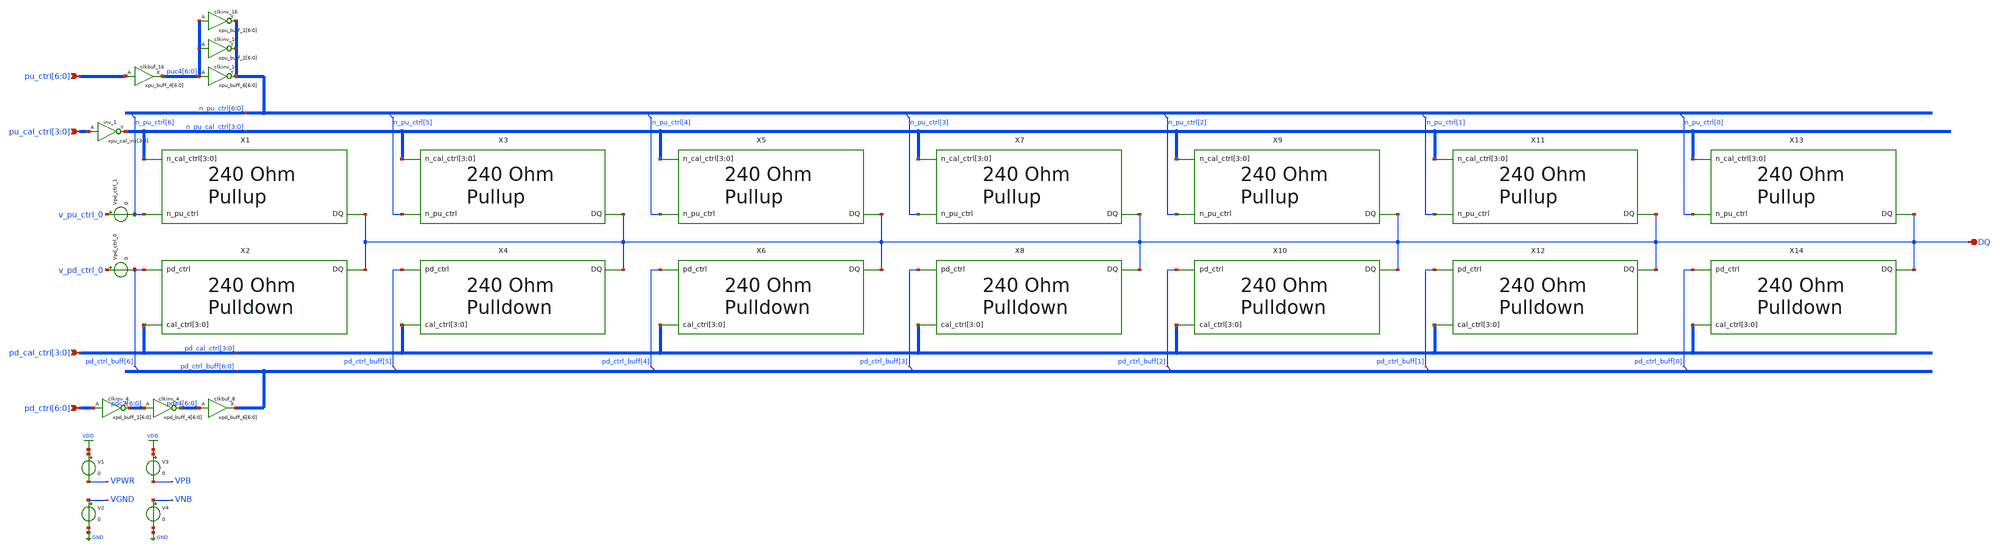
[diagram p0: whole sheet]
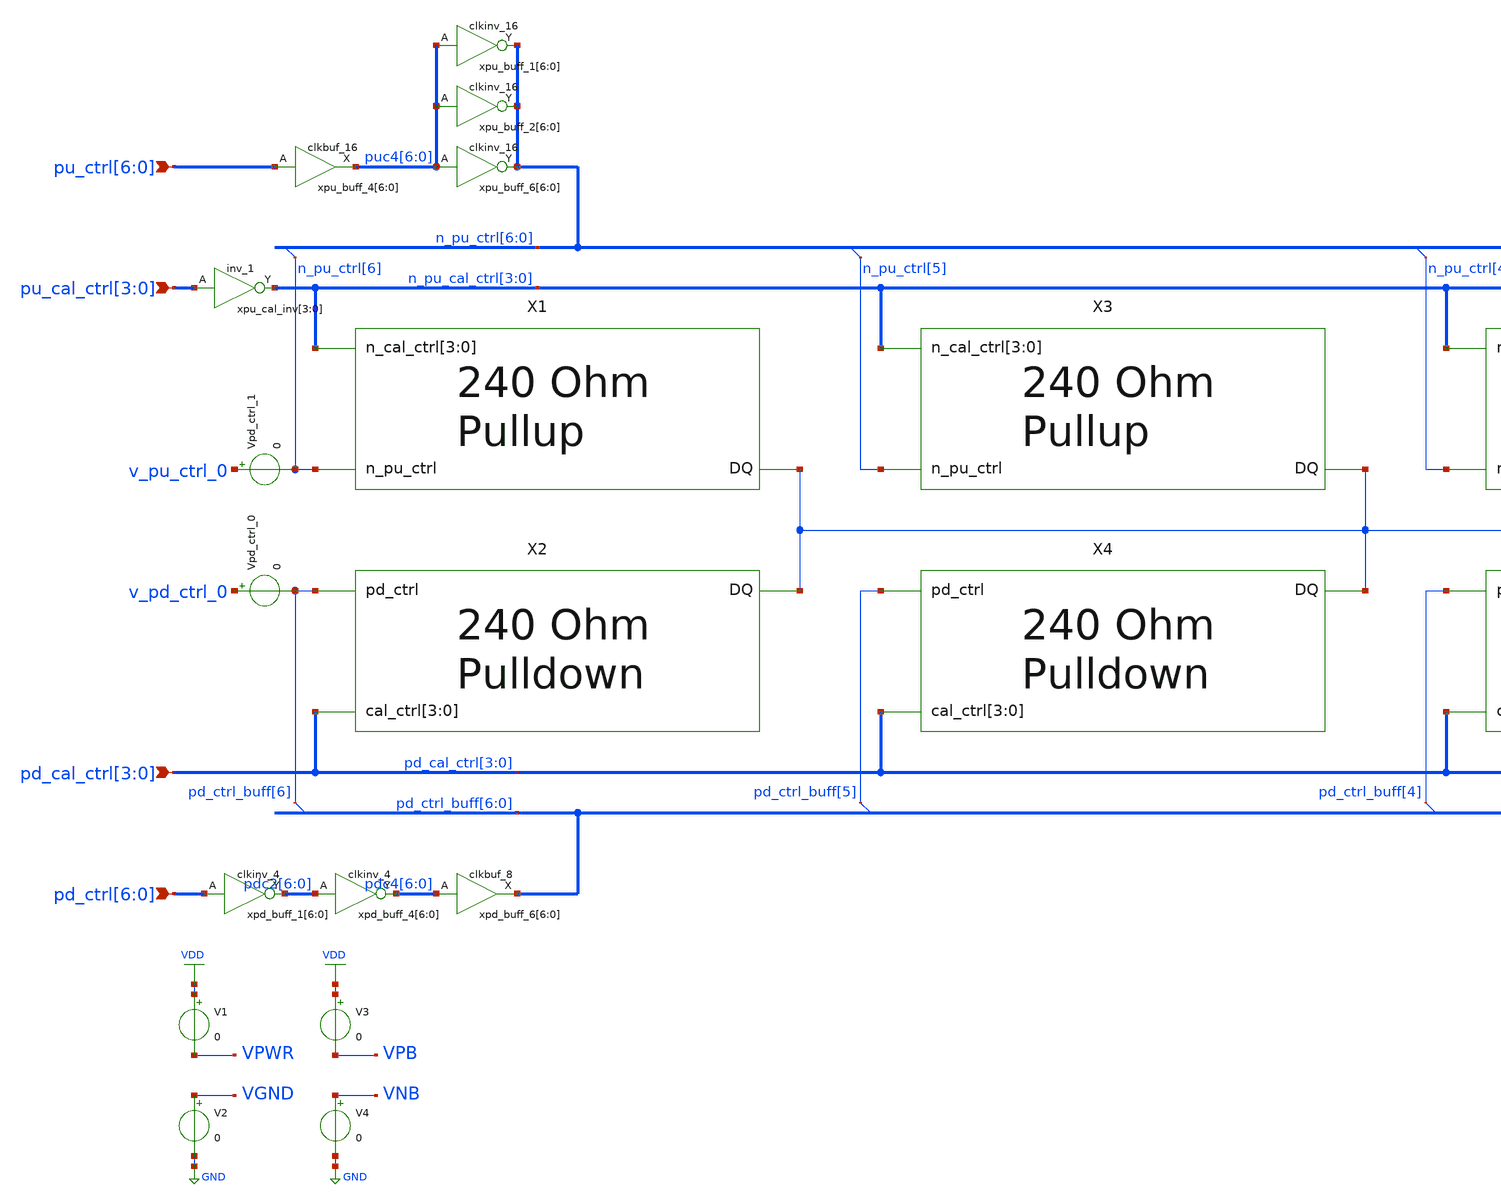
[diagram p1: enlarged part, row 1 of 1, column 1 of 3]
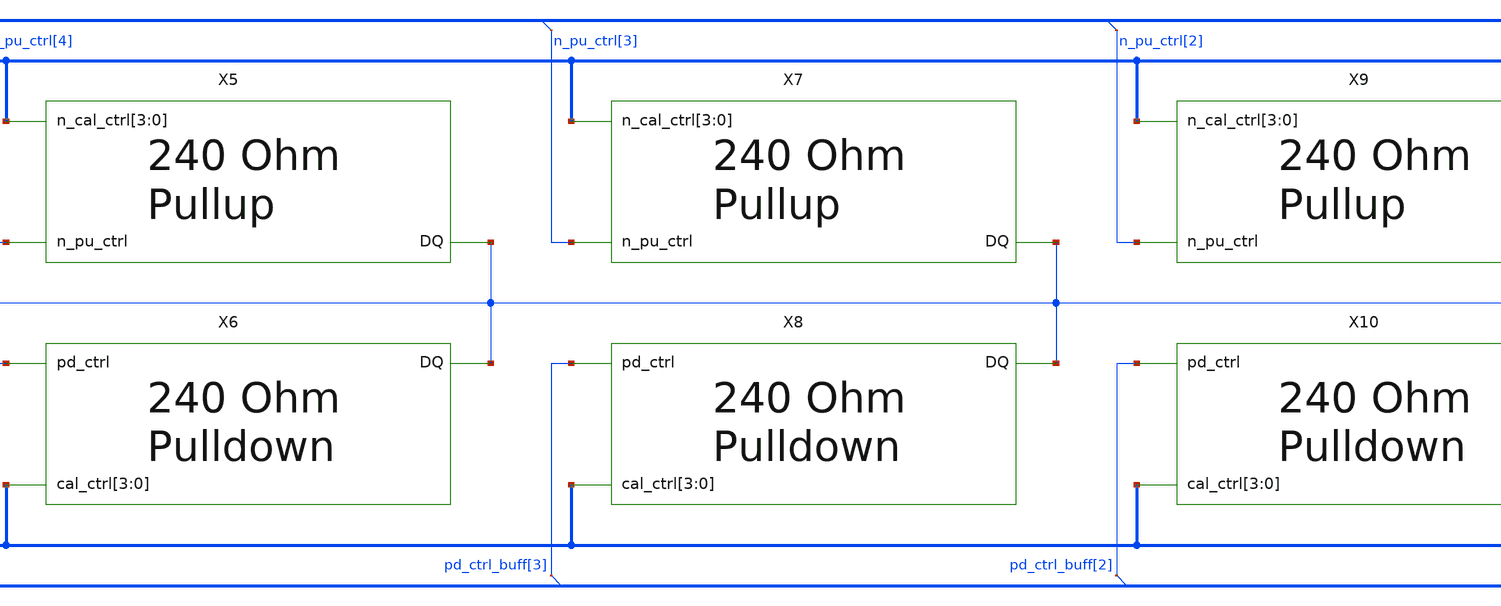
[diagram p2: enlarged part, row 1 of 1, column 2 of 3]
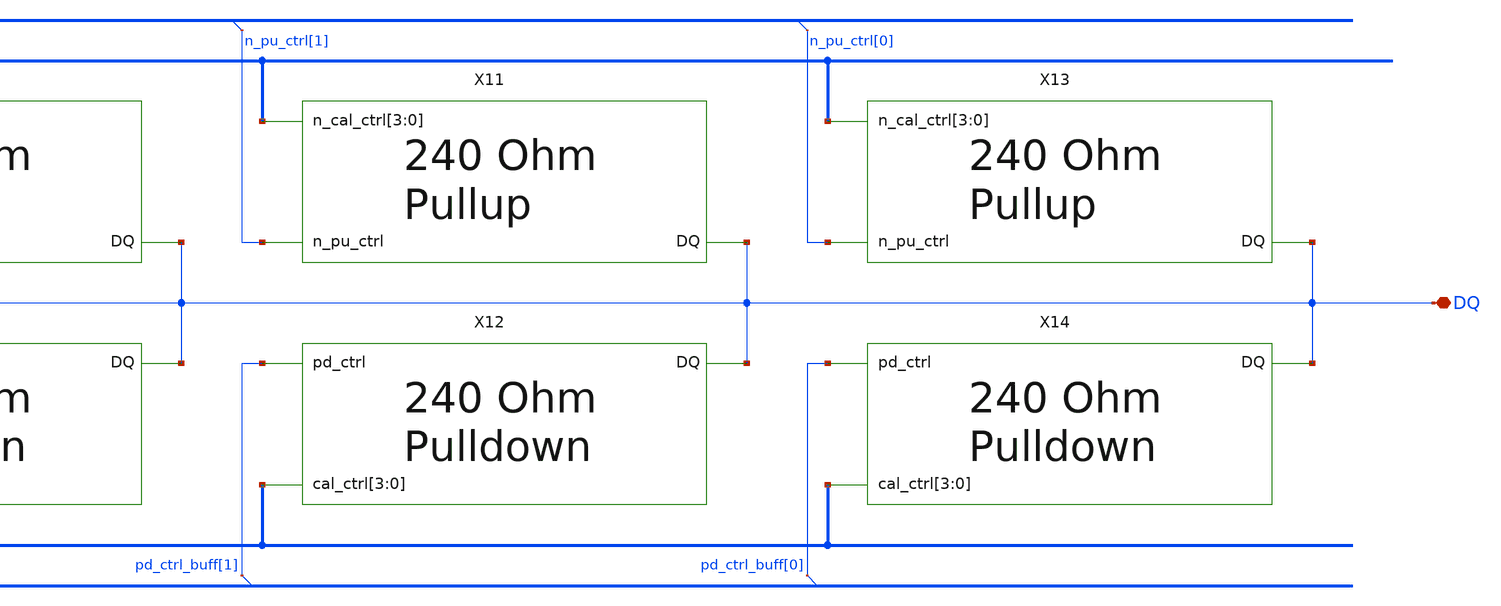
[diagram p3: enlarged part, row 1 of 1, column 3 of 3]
** sch_path: schem/SSTL.sch
* Copyright 2021 Stefan Frederik Schippers
* Licensed under the Apache License, Version 2.0 (the "License");
* you may not use this file except in compliance with the License.
* You may obtain a copy of the License at
* https://www.apache.org/licenses/LICENSE-2.0
* Unless required by applicable law or agreed to in writing, software
* distributed under the License is distributed on an "AS IS" BASIS,
* WITHOUT WARRANTIES OR CONDITIONS OF ANY KIND, either express or implied.
* See the License for the specific language governing permissions and
* limitations under the License.
**.subckt SSTL DQ pu_cal_ctrl[3],pu_cal_ctrl[2],pu_cal_ctrl[1],pu_cal_ctrl[0]
*+ pd_cal_ctrl[3],pd_cal_ctrl[2],pd_cal_ctrl[1],pd_cal_ctrl[0] pu_ctrl[6],pu_ctrl[5],pu_ctrl[4],pu_ctrl[3],pu_ctrl[2],pu_ctrl[1],pu_ctrl[0]
*+ pd_ctrl[6],pd_ctrl[5],pd_ctrl[4],pd_ctrl[3],pd_ctrl[2],pd_ctrl[1],pd_ctrl[0]
*.iopin DQ
*.ipin pu_cal_ctrl[3],pu_cal_ctrl[2],pu_cal_ctrl[1],pu_cal_ctrl[0]
*.ipin pd_cal_ctrl[3],pd_cal_ctrl[2],pd_cal_ctrl[1],pd_cal_ctrl[0]
*.ipin pu_ctrl[6],pu_ctrl[5],pu_ctrl[4],pu_ctrl[3],pu_ctrl[2],pu_ctrl[1],pu_ctrl[0]
*.ipin pd_ctrl[6],pd_ctrl[5],pd_ctrl[4],pd_ctrl[3],pd_ctrl[2],pd_ctrl[1],pd_ctrl[0]
X1 DQ n_pu_ctrl[6] n_pu_cal_ctrl[3] n_pu_cal_ctrl[2] n_pu_cal_ctrl[1] n_pu_cal_ctrl[0] p-leg
X2 DQ pd_ctrl_buff[6] pd_cal_ctrl[3] pd_cal_ctrl[2] pd_cal_ctrl[1] pd_cal_ctrl[0] n-leg
X3 DQ n_pu_ctrl[5] n_pu_cal_ctrl[3] n_pu_cal_ctrl[2] n_pu_cal_ctrl[1] n_pu_cal_ctrl[0] p-leg
X4 DQ pd_ctrl_buff[5] pd_cal_ctrl[3] pd_cal_ctrl[2] pd_cal_ctrl[1] pd_cal_ctrl[0] n-leg
X5 DQ n_pu_ctrl[4] n_pu_cal_ctrl[3] n_pu_cal_ctrl[2] n_pu_cal_ctrl[1] n_pu_cal_ctrl[0] p-leg
X6 DQ pd_ctrl_buff[4] pd_cal_ctrl[3] pd_cal_ctrl[2] pd_cal_ctrl[1] pd_cal_ctrl[0] n-leg
X7 DQ n_pu_ctrl[3] n_pu_cal_ctrl[3] n_pu_cal_ctrl[2] n_pu_cal_ctrl[1] n_pu_cal_ctrl[0] p-leg
X8 DQ pd_ctrl_buff[3] pd_cal_ctrl[3] pd_cal_ctrl[2] pd_cal_ctrl[1] pd_cal_ctrl[0] n-leg
X9 DQ n_pu_ctrl[2] n_pu_cal_ctrl[3] n_pu_cal_ctrl[2] n_pu_cal_ctrl[1] n_pu_cal_ctrl[0] p-leg
X10 DQ pd_ctrl_buff[2] pd_cal_ctrl[3] pd_cal_ctrl[2] pd_cal_ctrl[1] pd_cal_ctrl[0] n-leg
X11 DQ n_pu_ctrl[1] n_pu_cal_ctrl[3] n_pu_cal_ctrl[2] n_pu_cal_ctrl[1] n_pu_cal_ctrl[0] p-leg
X12 DQ pd_ctrl_buff[1] pd_cal_ctrl[3] pd_cal_ctrl[2] pd_cal_ctrl[1] pd_cal_ctrl[0] n-leg
X13 DQ n_pu_ctrl[0] n_pu_cal_ctrl[3] n_pu_cal_ctrl[2] n_pu_cal_ctrl[1] n_pu_cal_ctrl[0] p-leg
X14 DQ pd_ctrl_buff[0] pd_cal_ctrl[3] pd_cal_ctrl[2] pd_cal_ctrl[1] pd_cal_ctrl[0] n-leg
xpd_buff_4[6] pdc2[6] VGND VNB VPB VPWR pdc4[6] sky130_fd_sc_hd__clkinv_4
xpd_buff_4[5] pdc2[5] VGND VNB VPB VPWR pdc4[5] sky130_fd_sc_hd__clkinv_4
xpd_buff_4[4] pdc2[4] VGND VNB VPB VPWR pdc4[4] sky130_fd_sc_hd__clkinv_4
xpd_buff_4[3] pdc2[3] VGND VNB VPB VPWR pdc4[3] sky130_fd_sc_hd__clkinv_4
xpd_buff_4[2] pdc2[2] VGND VNB VPB VPWR pdc4[2] sky130_fd_sc_hd__clkinv_4
xpd_buff_4[1] pdc2[1] VGND VNB VPB VPWR pdc4[1] sky130_fd_sc_hd__clkinv_4
xpd_buff_4[0] pdc2[0] VGND VNB VPB VPWR pdc4[0] sky130_fd_sc_hd__clkinv_4
xpd_buff_6[6] pdc4[6] VGND VNB VPB VPWR pd_ctrl_buff[6] sky130_fd_sc_hd__clkbuf_8
xpd_buff_6[5] pdc4[5] VGND VNB VPB VPWR pd_ctrl_buff[5] sky130_fd_sc_hd__clkbuf_8
xpd_buff_6[4] pdc4[4] VGND VNB VPB VPWR pd_ctrl_buff[4] sky130_fd_sc_hd__clkbuf_8
xpd_buff_6[3] pdc4[3] VGND VNB VPB VPWR pd_ctrl_buff[3] sky130_fd_sc_hd__clkbuf_8
xpd_buff_6[2] pdc4[2] VGND VNB VPB VPWR pd_ctrl_buff[2] sky130_fd_sc_hd__clkbuf_8
xpd_buff_6[1] pdc4[1] VGND VNB VPB VPWR pd_ctrl_buff[1] sky130_fd_sc_hd__clkbuf_8
xpd_buff_6[0] pdc4[0] VGND VNB VPB VPWR pd_ctrl_buff[0] sky130_fd_sc_hd__clkbuf_8
xpu_buff_4[6] pu_ctrl[6] VGND VNB VPB VPWR puc4[6] sky130_fd_sc_hd__clkbuf_16
xpu_buff_4[5] pu_ctrl[5] VGND VNB VPB VPWR puc4[5] sky130_fd_sc_hd__clkbuf_16
xpu_buff_4[4] pu_ctrl[4] VGND VNB VPB VPWR puc4[4] sky130_fd_sc_hd__clkbuf_16
xpu_buff_4[3] pu_ctrl[3] VGND VNB VPB VPWR puc4[3] sky130_fd_sc_hd__clkbuf_16
xpu_buff_4[2] pu_ctrl[2] VGND VNB VPB VPWR puc4[2] sky130_fd_sc_hd__clkbuf_16
xpu_buff_4[1] pu_ctrl[1] VGND VNB VPB VPWR puc4[1] sky130_fd_sc_hd__clkbuf_16
xpu_buff_4[0] pu_ctrl[0] VGND VNB VPB VPWR puc4[0] sky130_fd_sc_hd__clkbuf_16
xpu_buff_6[6] puc4[6] VGND VNB VPB VPWR n_pu_ctrl[6] sky130_fd_sc_hd__clkinv_16
xpu_buff_6[5] puc4[5] VGND VNB VPB VPWR n_pu_ctrl[5] sky130_fd_sc_hd__clkinv_16
xpu_buff_6[4] puc4[4] VGND VNB VPB VPWR n_pu_ctrl[4] sky130_fd_sc_hd__clkinv_16
xpu_buff_6[3] puc4[3] VGND VNB VPB VPWR n_pu_ctrl[3] sky130_fd_sc_hd__clkinv_16
xpu_buff_6[2] puc4[2] VGND VNB VPB VPWR n_pu_ctrl[2] sky130_fd_sc_hd__clkinv_16
xpu_buff_6[1] puc4[1] VGND VNB VPB VPWR n_pu_ctrl[1] sky130_fd_sc_hd__clkinv_16
xpu_buff_6[0] puc4[0] VGND VNB VPB VPWR n_pu_ctrl[0] sky130_fd_sc_hd__clkinv_16
xpu_cal_inv[3] pu_cal_ctrl[3] VGND VNB VPB VPWR n_pu_cal_ctrl[3] sky130_fd_sc_hd__inv_1
xpu_cal_inv[2] pu_cal_ctrl[2] VGND VNB VPB VPWR n_pu_cal_ctrl[2] sky130_fd_sc_hd__inv_1
xpu_cal_inv[1] pu_cal_ctrl[1] VGND VNB VPB VPWR n_pu_cal_ctrl[1] sky130_fd_sc_hd__inv_1
xpu_cal_inv[0] pu_cal_ctrl[0] VGND VNB VPB VPWR n_pu_cal_ctrl[0] sky130_fd_sc_hd__inv_1
V1 VDD VPWR 0
V2 VGND GND 0
V3 VDD VPB 0
V4 VNB GND 0
Vpd_ctrl_0 v_pd_ctrl_0 pd_ctrl_buff[6] 0
Vpd_ctrl_1 v_pu_ctrl_0 n_pu_ctrl[6] 0
xpu_buff_2[6] puc4[6] VGND VNB VPB VPWR n_pu_ctrl[6] sky130_fd_sc_hd__clkinv_16
xpu_buff_2[5] puc4[5] VGND VNB VPB VPWR n_pu_ctrl[5] sky130_fd_sc_hd__clkinv_16
xpu_buff_2[4] puc4[4] VGND VNB VPB VPWR n_pu_ctrl[4] sky130_fd_sc_hd__clkinv_16
xpu_buff_2[3] puc4[3] VGND VNB VPB VPWR n_pu_ctrl[3] sky130_fd_sc_hd__clkinv_16
xpu_buff_2[2] puc4[2] VGND VNB VPB VPWR n_pu_ctrl[2] sky130_fd_sc_hd__clkinv_16
xpu_buff_2[1] puc4[1] VGND VNB VPB VPWR n_pu_ctrl[1] sky130_fd_sc_hd__clkinv_16
xpu_buff_2[0] puc4[0] VGND VNB VPB VPWR n_pu_ctrl[0] sky130_fd_sc_hd__clkinv_16
xpd_buff_1[6] pd_ctrl[6] VGND VNB VPB VPWR pdc2[6] sky130_fd_sc_hd__clkinv_4
xpd_buff_1[5] pd_ctrl[5] VGND VNB VPB VPWR pdc2[5] sky130_fd_sc_hd__clkinv_4
xpd_buff_1[4] pd_ctrl[4] VGND VNB VPB VPWR pdc2[4] sky130_fd_sc_hd__clkinv_4
xpd_buff_1[3] pd_ctrl[3] VGND VNB VPB VPWR pdc2[3] sky130_fd_sc_hd__clkinv_4
xpd_buff_1[2] pd_ctrl[2] VGND VNB VPB VPWR pdc2[2] sky130_fd_sc_hd__clkinv_4
xpd_buff_1[1] pd_ctrl[1] VGND VNB VPB VPWR pdc2[1] sky130_fd_sc_hd__clkinv_4
xpd_buff_1[0] pd_ctrl[0] VGND VNB VPB VPWR pdc2[0] sky130_fd_sc_hd__clkinv_4
xpu_buff_1[6] puc4[6] VGND VNB VPB VPWR n_pu_ctrl[6] sky130_fd_sc_hd__clkinv_16
xpu_buff_1[5] puc4[5] VGND VNB VPB VPWR n_pu_ctrl[5] sky130_fd_sc_hd__clkinv_16
xpu_buff_1[4] puc4[4] VGND VNB VPB VPWR n_pu_ctrl[4] sky130_fd_sc_hd__clkinv_16
xpu_buff_1[3] puc4[3] VGND VNB VPB VPWR n_pu_ctrl[3] sky130_fd_sc_hd__clkinv_16
xpu_buff_1[2] puc4[2] VGND VNB VPB VPWR n_pu_ctrl[2] sky130_fd_sc_hd__clkinv_16
xpu_buff_1[1] puc4[1] VGND VNB VPB VPWR n_pu_ctrl[1] sky130_fd_sc_hd__clkinv_16
xpu_buff_1[0] puc4[0] VGND VNB VPB VPWR n_pu_ctrl[0] sky130_fd_sc_hd__clkinv_16
**.ends

* expanding   symbol:  p-leg.sym # of pins=3
** sym_path: schem/p-leg.sym
** sch_path: schem/p-leg.sch
.subckt p-leg DQ n_pu_ctrl n_cal_ctrl[3] n_cal_ctrl[2] n_cal_ctrl[1] n_cal_ctrl[0]
*.ipin n_cal_ctrl[3],n_cal_ctrl[2],n_cal_ctrl[1],n_cal_ctrl[0]
*.ipin n_pu_ctrl
*.iopin DQ
XR1 DQ net1 sky130_fd_pr__res_generic_po W=0.33 L=1.8 m=1
XMpullup net1 n_pu_ctrl VDD VDD sky130_fd_pr__pfet_01v8_lvt L=0.35 W=1 nf=1 ad='int((nf+1)/2) * W/nf * 0.29'
+ as='int((nf+2)/2) * W/nf * 0.29' pd='2*int((nf+1)/2) * (W/nf + 0.29)' ps='2*int((nf+2)/2) * (W/nf + 0.29)'
+ nrd='0.29 / W' nrs='0.29 / W' sa=0 sb=0 sd=0 mult=128 m=128
XMctrltot VDD n_cal_ctrl[0] VDD VDD sky130_fd_pr__pfet_01v8_lvt L=0.35 W=1 nf=1 ad='int((nf+1)/2) * W/nf * 0.29'
+ as='int((nf+2)/2) * W/nf * 0.29' pd='2*int((nf+1)/2) * (W/nf + 0.29)' ps='2*int((nf+2)/2) * (W/nf + 0.29)'
+ nrd='0.29 / W' nrs='0.29 / W' sa=0 sb=0 sd=0 mult=120 m=120
XMctrl0 DQ n_cal_ctrl[0] net1 VDD sky130_fd_pr__pfet_01v8_lvt L=0.35 W=1 nf=1 ad='int((nf+1)/2) * W/nf * 0.29'
+ as='int((nf+2)/2) * W/nf * 0.29' pd='2*int((nf+1)/2) * (W/nf + 0.29)' ps='2*int((nf+2)/2) * (W/nf + 0.29)'
+ nrd='0.29 / W' nrs='0.29 / W' sa=0 sb=0 sd=0 mult=48 m=48
XMctrl1 DQ n_cal_ctrl[1] net1 VDD sky130_fd_pr__pfet_01v8_lvt L=0.35 W=1 nf=1 ad='int((nf+1)/2) * W/nf * 0.29'
+ as='int((nf+2)/2) * W/nf * 0.29' pd='2*int((nf+1)/2) * (W/nf + 0.29)' ps='2*int((nf+2)/2) * (W/nf + 0.29)'
+ nrd='0.29 / W' nrs='0.29 / W' sa=0 sb=0 sd=0 mult=16 m=16
XMctrl2 DQ n_cal_ctrl[2] net1 VDD sky130_fd_pr__pfet_01v8_lvt L=0.35 W=1 nf=1 ad='int((nf+1)/2) * W/nf * 0.29'
+ as='int((nf+2)/2) * W/nf * 0.29' pd='2*int((nf+1)/2) * (W/nf + 0.29)' ps='2*int((nf+2)/2) * (W/nf + 0.29)'
+ nrd='0.29 / W' nrs='0.29 / W' sa=0 sb=0 sd=0 mult=8 m=8
XMctrl3 DQ n_cal_ctrl[3] net1 VDD sky130_fd_pr__pfet_01v8_lvt L=0.35 W=1 nf=1 ad='int((nf+1)/2) * W/nf * 0.29'
+ as='int((nf+2)/2) * W/nf * 0.29' pd='2*int((nf+1)/2) * (W/nf + 0.29)' ps='2*int((nf+2)/2) * (W/nf + 0.29)'
+ nrd='0.29 / W' nrs='0.29 / W' sa=0 sb=0 sd=0 mult=4 m=4
.ends


* expanding   symbol:  n-leg.sym # of pins=3
** sym_path: schem/n-leg.sym
** sch_path: schem/n-leg.sch
.subckt n-leg DQ pd_ctrl cal_ctrl[3] cal_ctrl[2] cal_ctrl[1] cal_ctrl[0]
*.iopin DQ
*.ipin pd_ctrl
*.ipin cal_ctrl[3],cal_ctrl[2],cal_ctrl[1],cal_ctrl[0]
XR1 vpulldown DQ sky130_fd_pr__res_generic_po W=0.33 L=1.7 m=1
Xn1 vpulldown pd_ctrl GND GND sky130_fd_pr__nfet_01v8 L=0.15 W=0.65 nf=1 ad='int((nf+1)/2) * W/nf * 0.29'
+ as='int((nf+2)/2) * W/nf * 0.29' pd='2*int((nf+1)/2) * (W/nf + 0.29)' ps='2*int((nf+2)/2) * (W/nf + 0.29)'
+ nrd='0.29 / W' nrs='0.29 / W' sa=0 sb=0 sd=0 mult=48 m=48
Xnctrl0 DQ cal_ctrl[0] vpulldown GND sky130_fd_pr__nfet_01v8 L=0.15 W=0.65 nf=1 ad='int((nf+1)/2) * W/nf * 0.29'
+ as='int((nf+2)/2) * W/nf * 0.29' pd='2*int((nf+1)/2) * (W/nf + 0.29)' ps='2*int((nf+2)/2) * (W/nf + 0.29)'
+ nrd='0.29 / W' nrs='0.29 / W' sa=0 sb=0 sd=0 mult=6 m=6
Xnctrl1 DQ cal_ctrl[1] vpulldown GND sky130_fd_pr__nfet_01v8 L=0.15 W=0.65 nf=1 ad='int((nf+1)/2) * W/nf * 0.29'
+ as='int((nf+2)/2) * W/nf * 0.29' pd='2*int((nf+1)/2) * (W/nf + 0.29)' ps='2*int((nf+2)/2) * (W/nf + 0.29)'
+ nrd='0.29 / W' nrs='0.29 / W' sa=0 sb=0 sd=0 mult=3 m=3
Xnctrl2 DQ cal_ctrl[2] vpulldown GND sky130_fd_pr__nfet_01v8 L=0.15 W=0.975 nf=1 ad='int((nf+1)/2) * W/nf * 0.29'
+ as='int((nf+2)/2) * W/nf * 0.29' pd='2*int((nf+1)/2) * (W/nf + 0.29)' ps='2*int((nf+2)/2) * (W/nf + 0.29)'
+ nrd='0.29 / W' nrs='0.29 / W' sa=0 sb=0 sd=0 mult=1 m=1
Xnctrl3 DQ cal_ctrl[3] vpulldown GND sky130_fd_pr__nfet_01v8 L=0.15 W=0.5 nf=1 ad='int((nf+1)/2) * W/nf * 0.29'
+ as='int((nf+2)/2) * W/nf * 0.29' pd='2*int((nf+1)/2) * (W/nf + 0.29)' ps='2*int((nf+2)/2) * (W/nf + 0.29)'
+ nrd='0.29 / W' nrs='0.29 / W' sa=0 sb=0 sd=0 mult=1 m=1
Xnctrl_tot GND GND GND GND sky130_fd_pr__nfet_01v8 L=0.15 W=0.65 nf=1 ad='int((nf+1)/2) * W/nf * 0.29'
+ as='int((nf+2)/2) * W/nf * 0.29' pd='2*int((nf+1)/2) * (W/nf + 0.29)' ps='2*int((nf+2)/2) * (W/nf + 0.29)'
+ nrd='0.29 / W' nrs='0.29 / W' sa=0 sb=0 sd=0 mult=11 m=11
.ends

.GLOBAL VDD
.GLOBAL GND
.end
